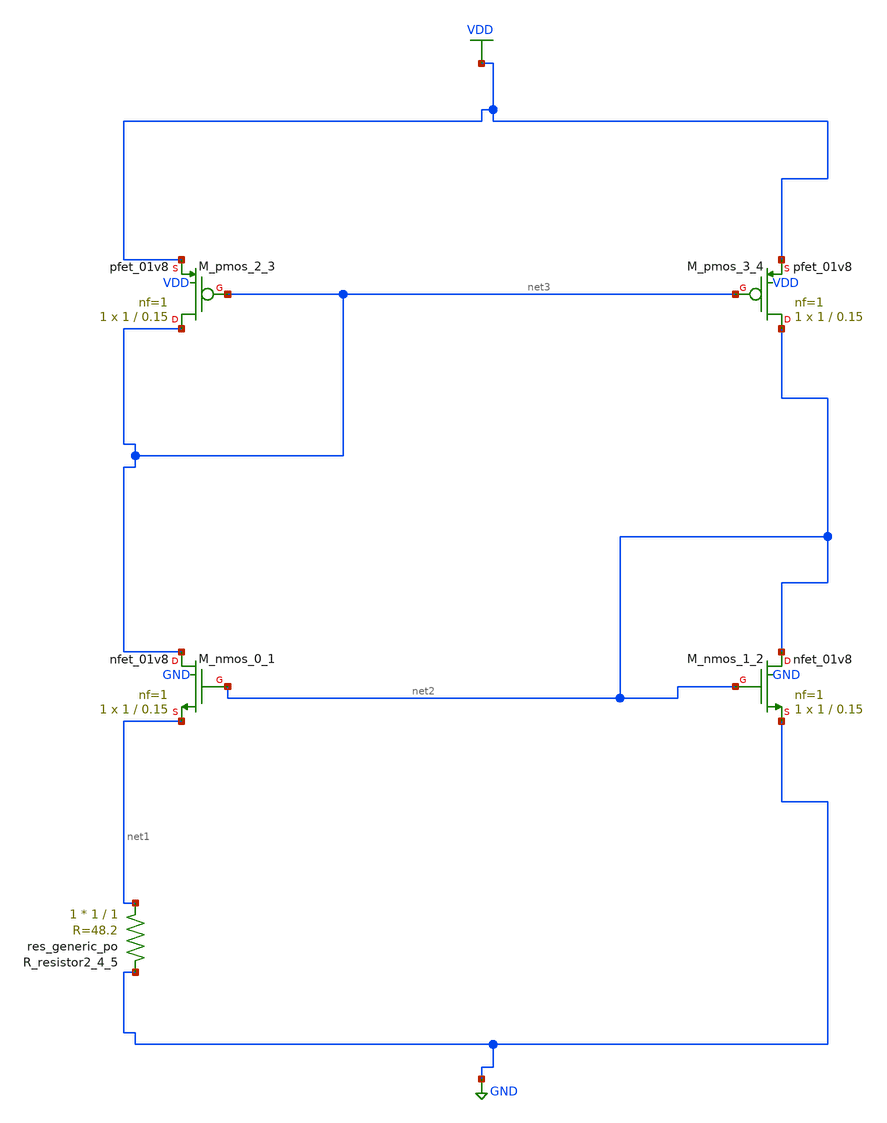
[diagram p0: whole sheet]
** sch_path: schematics/Image2Net/088.sch
**.subckt 088
XM_nmos_0_1 net3 net2 net1 GND sky130_fd_pr__nfet_01v8 L=0.15 W=1 nf=1 ad='int((1 + 1)/2) * 1 / 1 * 0.29'
+ as='int((1 + 2)/2) * 1 / 1 * 0.29' pd='2*int((1 + 1)/2) * (1 / 1 + 0.29)' ps='2*int((1 + 2)/2) * (1 / 1 + 0.29)'
+ nrd='0.29 / 1 ' nrs='0.29 / 1 ' sa=0 sb=0 sd=0 mult=1 m=1
XM_nmos_1_2 net2 net2 GND GND sky130_fd_pr__nfet_01v8 L=0.15 W=1 nf=1 ad='int((1 + 1)/2) * 1 / 1 * 0.29'
+ as='int((1 + 2)/2) * 1 / 1 * 0.29' pd='2*int((1 + 1)/2) * (1 / 1 + 0.29)' ps='2*int((1 + 2)/2) * (1 / 1 + 0.29)'
+ nrd='0.29 / 1 ' nrs='0.29 / 1 ' sa=0 sb=0 sd=0 mult=1 m=1
XM_pmos_2_3 net3 net3 VDD VDD sky130_fd_pr__pfet_01v8 L=0.15 W=1 nf=1 ad='int((1 + 1)/2) * 1 / 1 * 0.29'
+ as='int((1 + 2)/2) * 1 / 1 * 0.29' pd='2*int((1 + 1)/2) * (1 / 1 + 0.29)' ps='2*int((1 + 2)/2) * (1 / 1 + 0.29)'
+ nrd='0.29 / 1 ' nrs='0.29 / 1 ' sa=0 sb=0 sd=0 mult=1 m=1
XM_pmos_3_4 net2 net3 VDD VDD sky130_fd_pr__pfet_01v8 L=0.15 W=1 nf=1 ad='int((1 + 1)/2) * 1 / 1 * 0.29'
+ as='int((1 + 2)/2) * 1 / 1 * 0.29' pd='2*int((1 + 1)/2) * (1 / 1 + 0.29)' ps='2*int((1 + 2)/2) * (1 / 1 + 0.29)'
+ nrd='0.29 / 1 ' nrs='0.29 / 1 ' sa=0 sb=0 sd=0 mult=1 m=1
XR_resistor2_4_5 net1 GND sky130_fd_pr__res_generic_po W=1 L=1 m=1
**.ends
.GLOBAL GND
.GLOBAL VDD
.end
